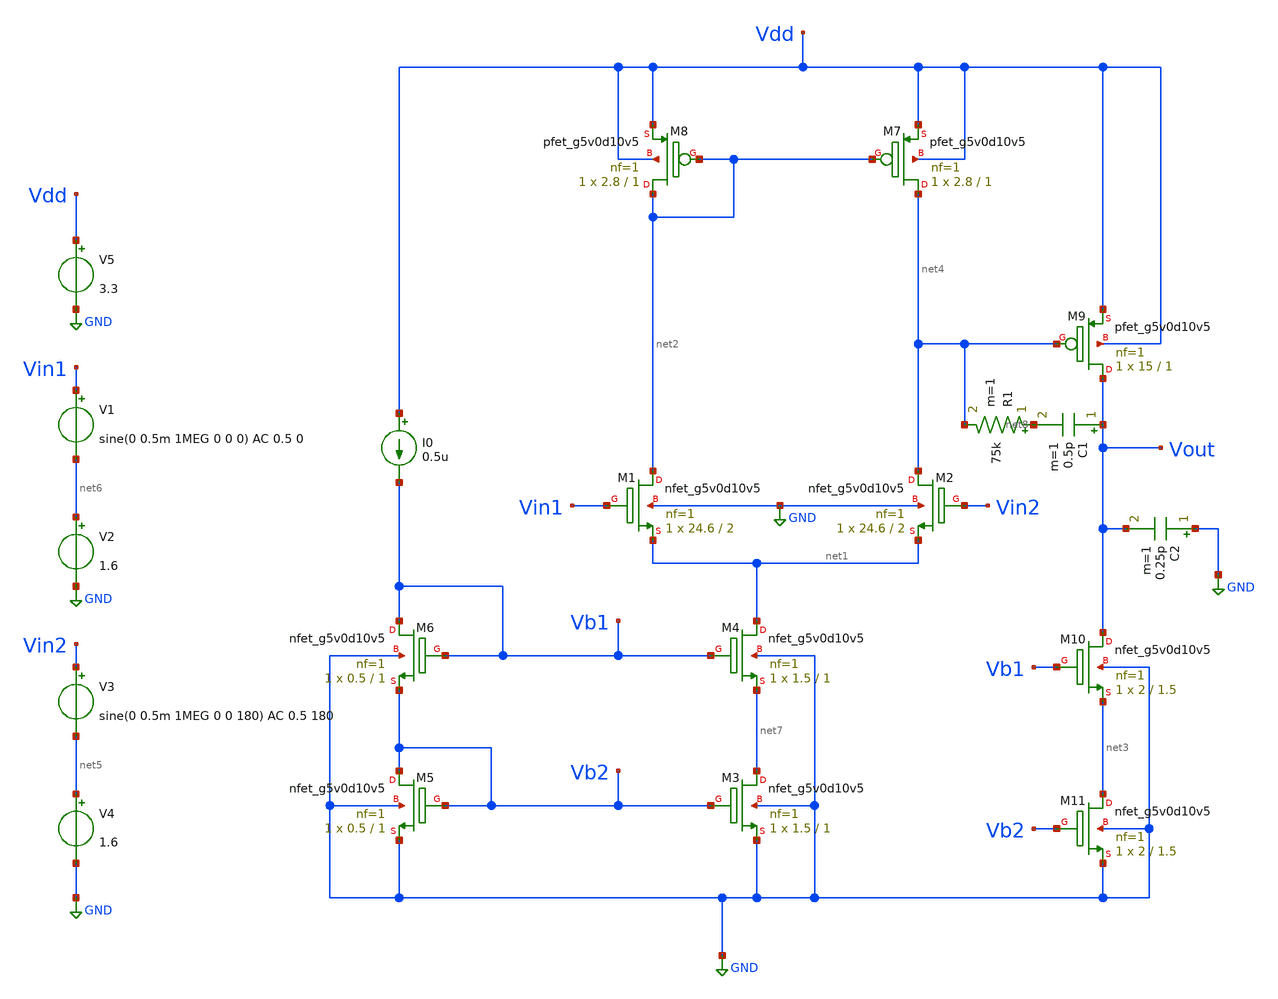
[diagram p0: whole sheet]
** sch_path: dacc.sch
**.subckt dacc
I0 Vdd Vb1 0.5u
C1 Vout net8 0.5p m=1
C2 GND Vout 0.25p m=1
V1 Vin1 net6 sine(0 0.5m 1MEG 0 0 0) AC 0.5 0
V2 net6 GND 1.6
V3 Vin2 net5 sine(0 0.5m 1MEG 0 0 180) AC 0.5 180
V4 net5 GND 1.6
V5 Vdd GND 3.3
R1 net8 net4 75k m=1
XM7 net4 net2 Vdd Vdd sky130_fd_pr__pfet_g5v0d10v5 L=1 W=2.8 nf=1 ad='int((1 + 1)/2) * 2.8 / 1 * 0.29'
+ as='int((1 + 2)/2) * 2.8 / 1 * 0.29' pd='2*int((1 + 1)/2) * (2.8 / 1 + 0.29)' ps='2*int((1 + 2)/2) * (2.8 / 1 + 0.29)'
+ nrd='0.29 / 2.8 ' nrs='0.29 / 2.8 ' sa=0 sb=0 sd=0 mult=1 m=1
XM8 net2 net2 Vdd Vdd sky130_fd_pr__pfet_g5v0d10v5 L=1 W=2.8 nf=1 ad='int((1 + 1)/2) * 2.8 / 1 * 0.29'
+ as='int((1 + 2)/2) * 2.8 / 1 * 0.29' pd='2*int((1 + 1)/2) * (2.8 / 1 + 0.29)' ps='2*int((1 + 2)/2) * (2.8 / 1 + 0.29)'
+ nrd='0.29 / 2.8 ' nrs='0.29 / 2.8 ' sa=0 sb=0 sd=0 mult=1 m=1
XM9 Vout net4 Vdd Vdd sky130_fd_pr__pfet_g5v0d10v5 L=1 W=15 nf=1 ad='int((1 + 1)/2) * 15 / 1 * 0.29'
+ as='int((1 + 2)/2) * 15 / 1 * 0.29' pd='2*int((1 + 1)/2) * (15 / 1 + 0.29)' ps='2*int((1 + 2)/2) * (15 / 1 + 0.29)'
+ nrd='0.29 / 15 ' nrs='0.29 / 15 ' sa=0 sb=0 sd=0 mult=1 m=1
XM10 Vout Vb1 net3 GND sky130_fd_pr__nfet_g5v0d10v5 L=1.5 W=2 nf=1 ad='int((1 + 1)/2) * 2 / 1 * 0.29'
+ as='int((1 + 2)/2) * 2 / 1 * 0.29' pd='2*int((1 + 1)/2) * (2 / 1 + 0.29)' ps='2*int((1 + 2)/2) * (2 / 1 + 0.29)'
+ nrd='0.29 / 2 ' nrs='0.29 / 2 ' sa=0 sb=0 sd=0 mult=1 m=1
XM11 net3 Vb2 GND GND sky130_fd_pr__nfet_g5v0d10v5 L=1.5 W=2 nf=1 ad='int((1 + 1)/2) * 2 / 1 * 0.29'
+ as='int((1 + 2)/2) * 2 / 1 * 0.29' pd='2*int((1 + 1)/2) * (2 / 1 + 0.29)' ps='2*int((1 + 2)/2) * (2 / 1 + 0.29)'
+ nrd='0.29 / 2 ' nrs='0.29 / 2 ' sa=0 sb=0 sd=0 mult=1 m=1
XM3 net7 Vb2 GND GND sky130_fd_pr__nfet_g5v0d10v5 L=1 W=1.5 nf=1 ad='int((1 + 1)/2) * 1.5 / 1 * 0.29'
+ as='int((1 + 2)/2) * 1.5 / 1 * 0.29' pd='2*int((1 + 1)/2) * (1.5 / 1 + 0.29)' ps='2*int((1 + 2)/2) * (1.5 / 1 + 0.29)'
+ nrd='0.29 / 1.5 ' nrs='0.29 / 1.5 ' sa=0 sb=0 sd=0 mult=1 m=1
XM4 net1 Vb1 net7 GND sky130_fd_pr__nfet_g5v0d10v5 L=1 W=1.5 nf=1 ad='int((1 + 1)/2) * 1.5 / 1 * 0.29'
+ as='int((1 + 2)/2) * 1.5 / 1 * 0.29' pd='2*int((1 + 1)/2) * (1.5 / 1 + 0.29)' ps='2*int((1 + 2)/2) * (1.5 / 1 + 0.29)'
+ nrd='0.29 / 1.5 ' nrs='0.29 / 1.5 ' sa=0 sb=0 sd=0 mult=1 m=1
XM5 Vb2 Vb2 GND GND sky130_fd_pr__nfet_g5v0d10v5 L=1 W=0.5 nf=1 ad='int((1 + 1)/2) * 0.5 / 1 * 0.29'
+ as='int((1 + 2)/2) * 0.5 / 1 * 0.29' pd='2*int((1 + 1)/2) * (0.5 / 1 + 0.29)' ps='2*int((1 + 2)/2) * (0.5 / 1 + 0.29)'
+ nrd='0.29 / 0.5 ' nrs='0.29 / 0.5 ' sa=0 sb=0 sd=0 mult=1 m=1
XM6 Vb1 Vb1 Vb2 GND sky130_fd_pr__nfet_g5v0d10v5 L=1 W=0.5 nf=1 ad='int((1 + 1)/2) * 0.5 / 1 * 0.29'
+ as='int((1 + 2)/2) * 0.5 / 1 * 0.29' pd='2*int((1 + 1)/2) * (0.5 / 1 + 0.29)' ps='2*int((1 + 2)/2) * (0.5 / 1 + 0.29)'
+ nrd='0.29 / 0.5 ' nrs='0.29 / 0.5 ' sa=0 sb=0 sd=0 mult=1 m=1
XM1 net2 Vin1 net1 GND sky130_fd_pr__nfet_g5v0d10v5 L=2 W=24.6 nf=1 ad='int((1 + 1)/2) * 24.6 / 1 * 0.29'
+ as='int((1 + 2)/2) * 24.6 / 1 * 0.29' pd='2*int((1 + 1)/2) * (24.6 / 1 + 0.29)' ps='2*int((1 + 2)/2) * (24.6 / 1 + 0.29)'
+ nrd='0.29 / 24.6 ' nrs='0.29 / 24.6 ' sa=0 sb=0 sd=0 mult=1 m=1
XM2 net4 Vin2 net1 GND sky130_fd_pr__nfet_g5v0d10v5 L=2 W=24.6 nf=1 ad='int((1 + 1)/2) * 24.6 / 1 * 0.29'
+ as='int((1 + 2)/2) * 24.6 / 1 * 0.29' pd='2*int((1 + 1)/2) * (24.6 / 1 + 0.29)' ps='2*int((1 + 2)/2) * (24.6 / 1 + 0.29)'
+ nrd='0.29 / 24.6 ' nrs='0.29 / 24.6 ' sa=0 sb=0 sd=0 mult=1 m=1
**** begin user architecture code


.lib /usr/local/share/pdk/sky130A/libs.tech/ngspice/sky130.lib.spice tt

.control
set color0=white
set color1=black

* 1. TRANSIENT SIMULATION
tran 10n 5u
plot v(vin1) v(vout)

* 2. AC FREQUENCY SWEEP & MEASUREMENTS
ac dec 20 1 1G

let g_db = db(v(vout))
let p_deg = (180/PI)*cph(v(vout))

meas ac dc_gain find g_db at=1
meas ac gbw when g_db=0
meas ac p_at_gbw find p_deg when g_db=0

* 2. Correct Phase Margin formula matching Razavi Eq. (10.11):
let pm_raw = 180 + p_at_gbw
let true_pm = (pm_raw > 90) ? (180 - pm_raw) : pm_raw

print dc_gain gbw true_pm
let p_scaled = p_deg / 2
plot g_db p_scaled
.endc


**** end user architecture code
**.ends
.GLOBAL GND
.end
